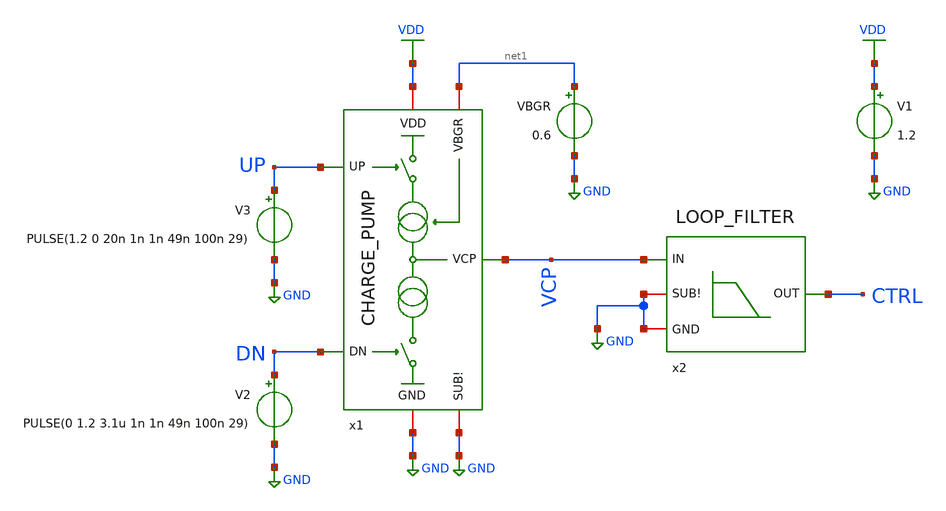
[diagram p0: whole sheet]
** sch_path: xschem/charge-pump/tb_CP_LF.sch
**.subckt tb_CP_LF
V1 VDD GND 1.2
V2 DN GND PULSE(0 1.2 3.1u 1n 1n 49n 100n 29)
V3 UP GND PULSE(1.2 0 20n 1n 1n 49n 100n 29)
VBGR net1 GND 0.6
x1 UP VDD VCP net1 GND DN GND CHARGE_PUMP
x2 CTRL VCP GND GND LOOP_FILTER
**** begin user architecture code



.include tb_CP.save
.param temp=27
.option method=gear rshunt=1.0e12
.control
save all
op
write tb_CP_LF.raw
.endc




.lib cornerMOSlv.lib mos_tt
.lib cornerMOShv.lib mos_tt
.lib cornerRES.lib res_typ
.lib cornerCAP.lib cap_typ




.param temp = 27
.options method=gear rshunt=1.0e12

.control

* Save required signals
save v(UP) v(DN) v(VCP) v(CTRL)

* Long transient simulation
tran 1n 6u

* Measurements
meas tran ctrl_end find v(CTRL) at=6u
meas tran ctrl_max max v(CTRL)
meas tran ctrl_min min v(CTRL)
meas tran vcp_end find v(VCP) at=6u
meas tran vcp_max max v(VCP)
* supply current (negative = drawn from the source), power = 1.2 V x |idd|
meas tran idd avg i(V1) from=1u to=6u

write tb_CP_LF_tran.raw v(UP) v(DN) v(VCP) v(CTRL)

* Plot transient waveform
plot v(UP) v(DN) v(VCP) v(CTRL)
plot v(CTRL)

.endc



**** end user architecture code
**.ends
.GLOBAL VDD
.GLOBAL GND
.end
